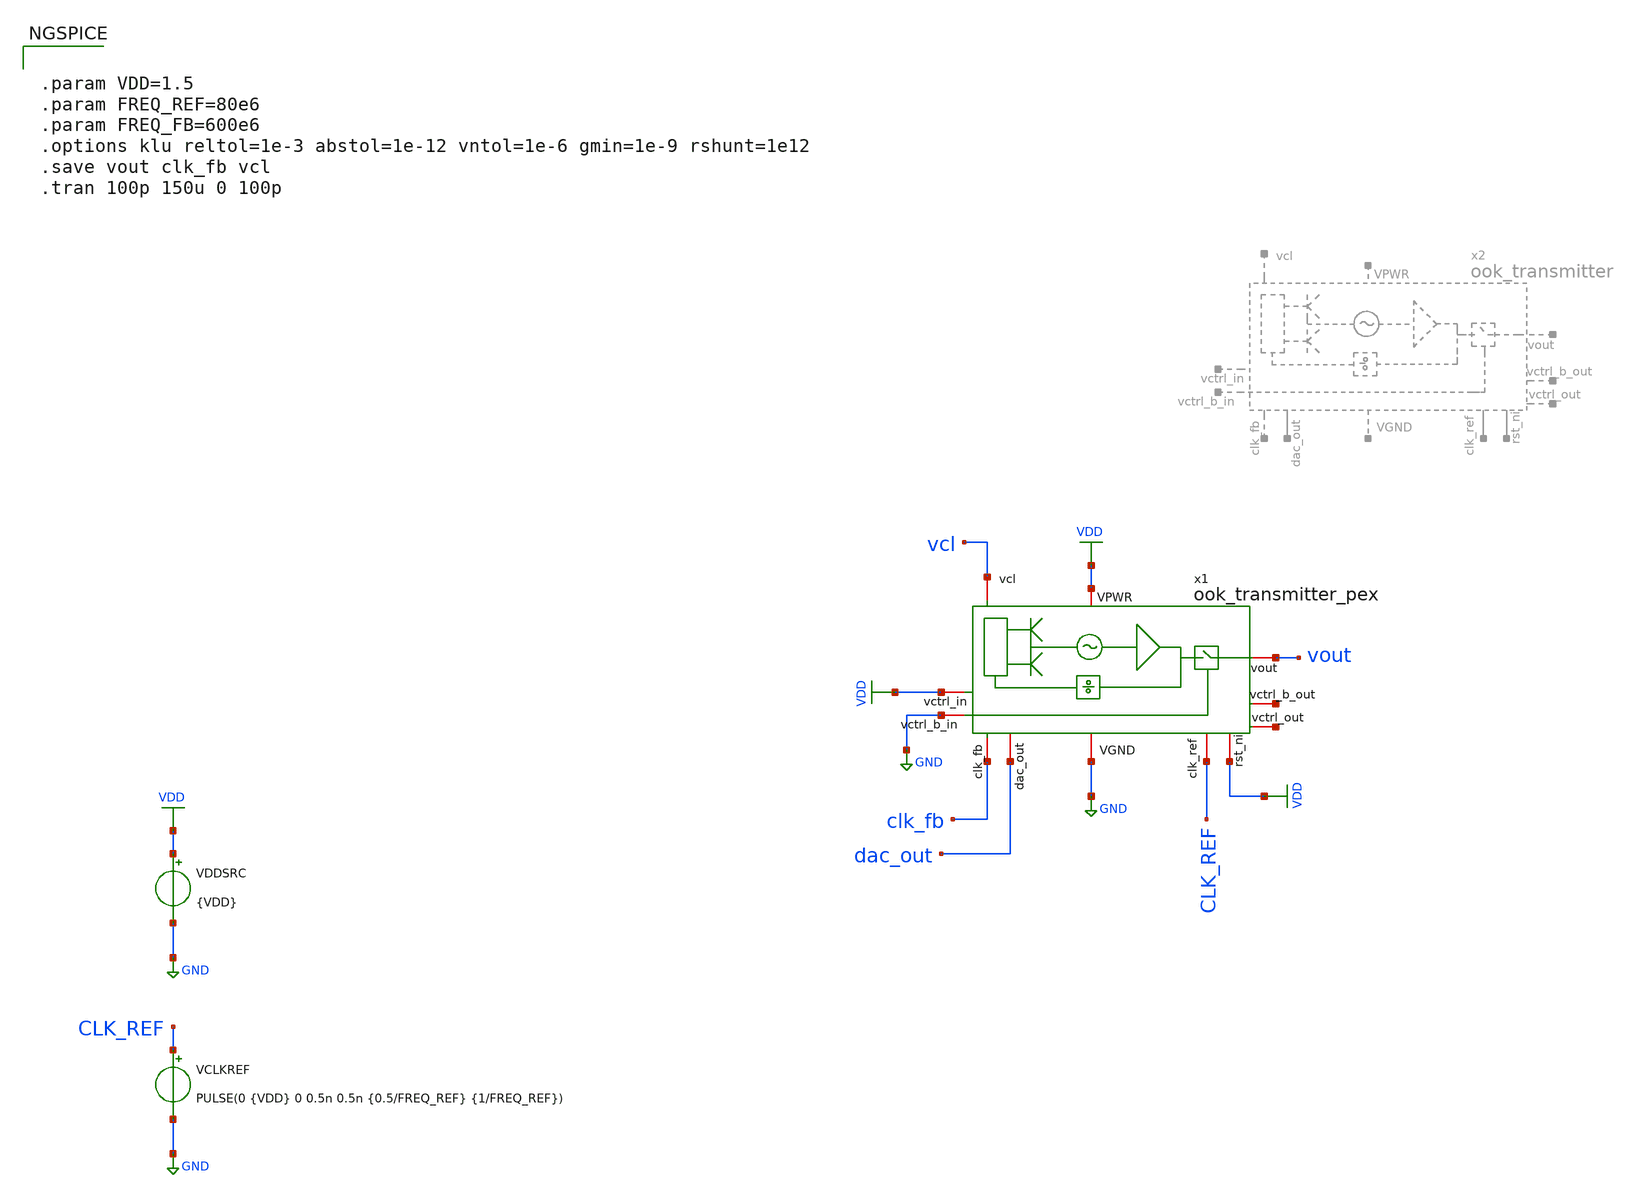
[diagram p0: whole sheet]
** sch_path: macros/heichips26_ook_top/macros/ook_analog_system/testbenches/xschem/ook_transmitter_tb_tran.sch
**.subckt ook_transmitter_tb_tran
VCLKREF CLK_REF GND PULSE(0 {VDD} 0 0.5n 0.5n {0.5/FREQ_REF} {1/FREQ_REF})
VDDSRC VDD GND {VDD}
x1 CLK_REF VDD VDD GND dac_out clk_fb vcl GND VDD vout net1 net2 ook_transmitter_pex
**** begin user architecture code


.param VDD=1.5
.param FREQ_REF=80e6
.param FREQ_FB=600e6
.options klu reltol=1e-3 abstol=1e-12 vntol=1e-6 gmin=1e-9 rshunt=1e12
.save vout clk_fb vcl
.tran 100p 150u 0 100p



.lib cornerMOSlv.lib mos_tt
.lib cornerMOShv.lib mos_tt
.lib cornerRES.lib res_typ
.lib cornerDIO.lib dio_tt
.lib cornerCAP.lib cap_typ
.include /home/belal/HeiChips/heichips26-on-off/macros/heichips26_ook_top/macros/dac/netlist/xspice/dac.xspice
.include /home/belal/HeiChips/heichips26-on-off/macros/heichips26_ook_top/macros/ook_analog_system/netlist/pex/ook_transmitter_magic_pex_3.spice
.include /home/belal/HeiChips/heichips26-on-off/IHP-Open-PDK/ihp-sg13cmos5l/libs.tech/ngspice/models/cap_mfringe.lib
.include /home/belal/HeiChips/heichips26-on-off/macros/heichips26_ook_top/macros/ook_analog_system/netlist/pex/vco_magic_pex_3.spice
.include /home/belal/HeiChips/heichips26-on-off/macros/heichips26_ook_top/macros/ook_analog_system/netlist/pex/output_buffer_magic_pex_3.spice

**** end user architecture code
**.ends
.GLOBAL GND
.GLOBAL VDD
.end
